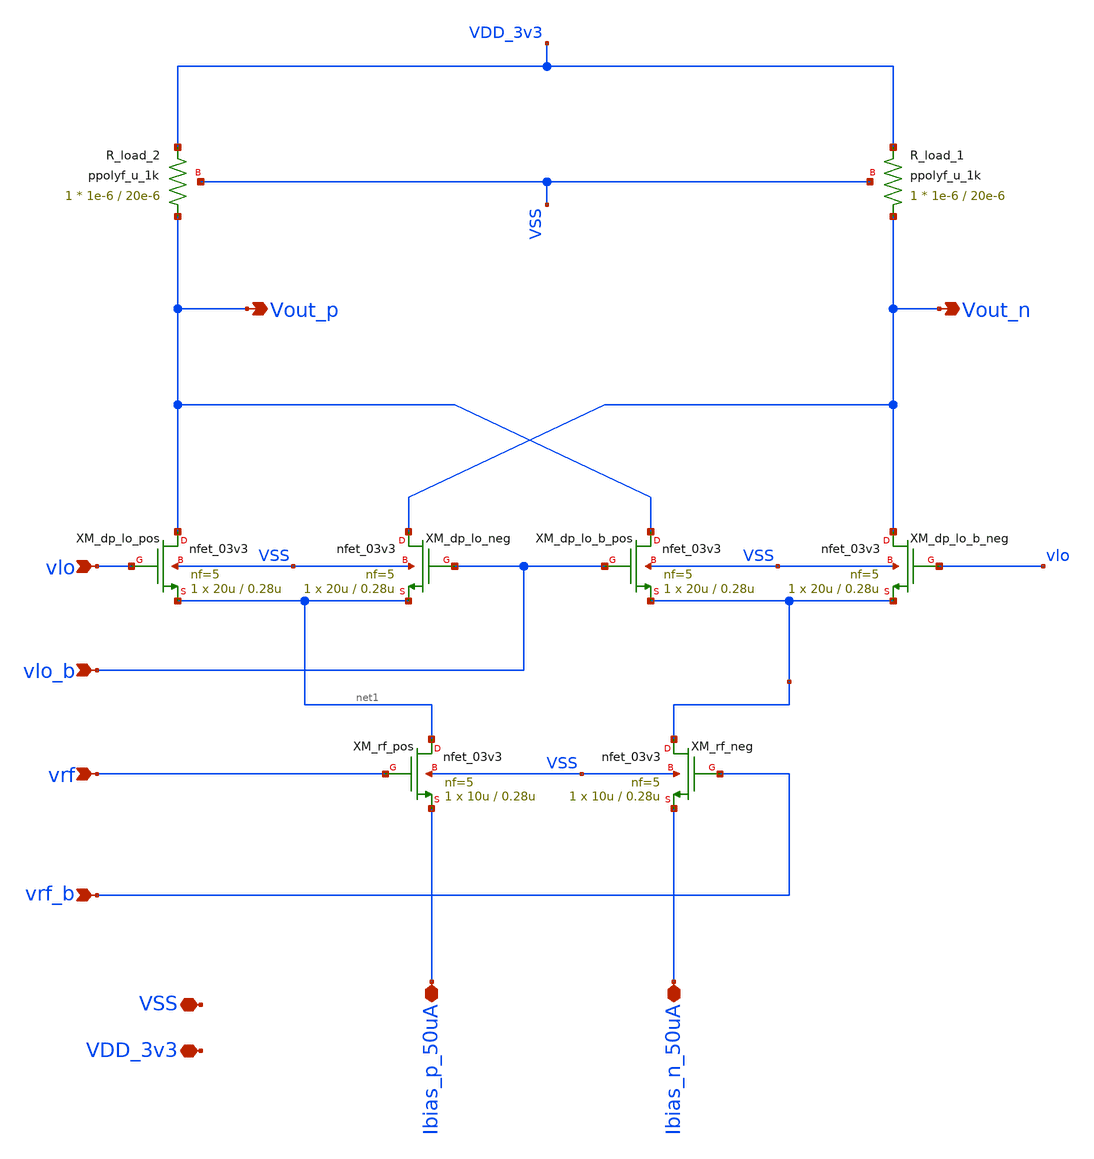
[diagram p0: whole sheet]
** sch_path: Analog/schematics/2_mixer/gilbert_mixer.sch
**.subckt gilbert_mixer vlo vlo_b vrf vrf_b Vout_p Vout_n Ibias_n_50uA Ibias_p_50uA VSS VDD_3v3
*.ipin vlo
*.ipin vlo_b
*.ipin vrf
*.ipin vrf_b
*.opin Vout_p
*.opin Vout_n
*.iopin Ibias_n_50uA
*.iopin Ibias_p_50uA
*.iopin VSS
*.iopin VDD_3v3
XM_dp_lo_pos Vout_p vlo net1 VSS nfet_03v3 L=0.28u W=20u nf=5 ad='int((nf+1)/2) * W/nf * 0.18u' as='int((nf+2)/2) * W/nf * 0.18u'
+ pd='2*int((nf+1)/2) * (W/nf + 0.18u)' ps='2*int((nf+2)/2) * (W/nf + 0.18u)' nrd='0.18u / W' nrs='0.18u / W'
+ sa=0 sb=0 sd=0 m=1
XM_dp_lo_neg Vout_n vlo_b net1 VSS nfet_03v3 L=0.28u W=20u nf=5 ad='int((nf+1)/2) * W/nf * 0.18u' as='int((nf+2)/2) * W/nf * 0.18u'
+ pd='2*int((nf+1)/2) * (W/nf + 0.18u)' ps='2*int((nf+2)/2) * (W/nf + 0.18u)' nrd='0.18u / W' nrs='0.18u / W'
+ sa=0 sb=0 sd=0 m=1
XM_dp_lo_b_pos Vout_p vlo_b rf_diff_pair_neg_input VSS nfet_03v3 L=0.28u W=20u nf=5 ad='int((nf+1)/2) * W/nf * 0.18u'
+ as='int((nf+2)/2) * W/nf * 0.18u' pd='2*int((nf+1)/2) * (W/nf + 0.18u)' ps='2*int((nf+2)/2) * (W/nf + 0.18u)'
+ nrd='0.18u / W' nrs='0.18u / W' sa=0 sb=0 sd=0 m=1
XM_dp_lo_b_neg Vout_n vlo rf_diff_pair_neg_input VSS nfet_03v3 L=0.28u W=20u nf=5 ad='int((nf+1)/2) * W/nf * 0.18u'
+ as='int((nf+2)/2) * W/nf * 0.18u' pd='2*int((nf+1)/2) * (W/nf + 0.18u)' ps='2*int((nf+2)/2) * (W/nf + 0.18u)'
+ nrd='0.18u / W' nrs='0.18u / W' sa=0 sb=0 sd=0 m=1
XM_rf_pos net1 vrf Ibias_p_50uA VSS nfet_03v3 L=0.28u W=10u nf=5 ad='int((nf+1)/2) * W/nf * 0.18u' as='int((nf+2)/2) * W/nf * 0.18u'
+ pd='2*int((nf+1)/2) * (W/nf + 0.18u)' ps='2*int((nf+2)/2) * (W/nf + 0.18u)' nrd='0.18u / W' nrs='0.18u / W'
+ sa=0 sb=0 sd=0 m=1
XM_rf_neg rf_diff_pair_neg_input vrf_b Ibias_n_50uA VSS nfet_03v3 L=0.28u W=10u nf=5 ad='int((nf+1)/2) * W/nf * 0.18u'
+ as='int((nf+2)/2) * W/nf * 0.18u' pd='2*int((nf+1)/2) * (W/nf + 0.18u)' ps='2*int((nf+2)/2) * (W/nf + 0.18u)'
+ nrd='0.18u / W' nrs='0.18u / W' sa=0 sb=0 sd=0 m=1
XR_load_2 Vout_p VDD_3v3 VSS ppolyf_u_1k r_width=1e-6 r_length=20e-6 m=1
XR_load_1 Vout_n VDD_3v3 VSS ppolyf_u_1k r_width=1e-6 r_length=20e-6 m=1
**.ends
.end
